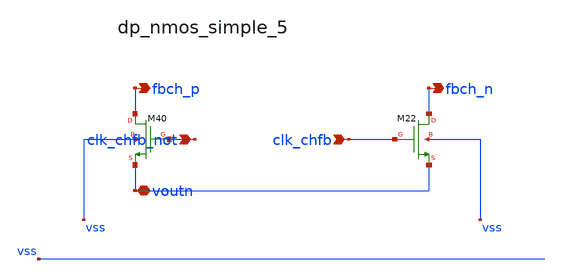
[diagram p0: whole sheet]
** sch_path: analog-db/raw/ia_003_fan_chopper_pf/hier/blocks/dp_nmos_simple_5.sch
**.subckt dp_nmos_simple_5 clk_chfb_not clk_chfb voutn fbch_p fbch_n
*.ipin clk_chfb_not
*.ipin clk_chfb
*.iopin voutn
*.opin fbch_p
*.opin fbch_n
XM22 fbch_n clk_chfb voutn vss sg13_lv_nmos w=x_dut_xm22_w l=x_dut_xm22_l ng=1 m=x_dut_xm22_m
XM40 fbch_p clk_chfb_not voutn vss sg13_lv_nmos w=x_dut_xm40_w l=x_dut_xm40_l ng=1 m=x_dut_xm40_m
**.ends
.end
